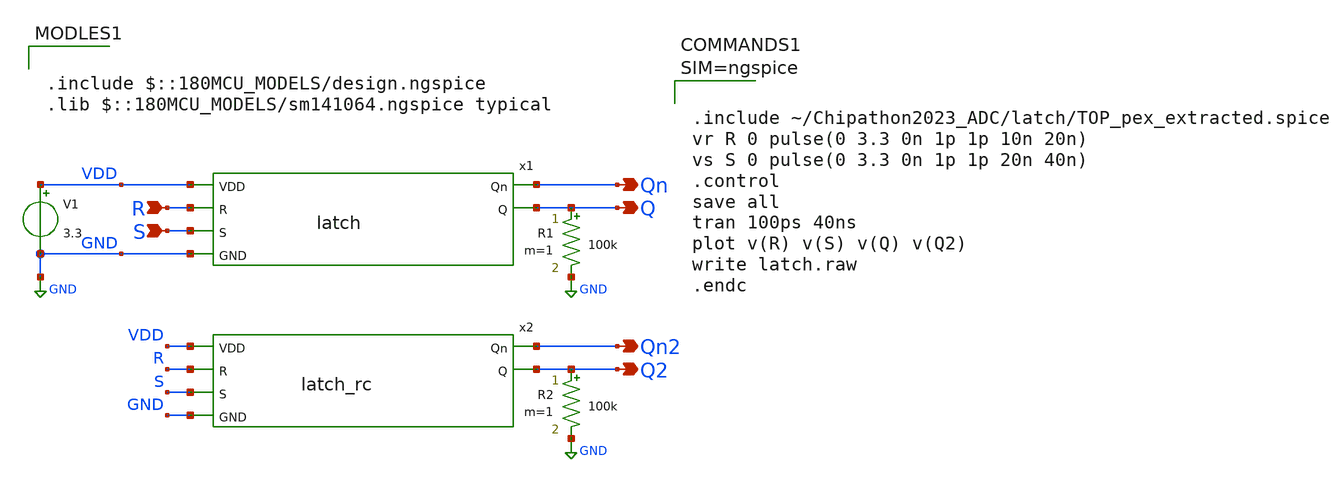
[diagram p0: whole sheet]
** sch_path: review/0407/latch/latch_rc_test.sch
**.subckt latch_rc_test Q R S Qn Q2 Qn2
*.opin Q
*.ipin R
*.ipin S
*.opin Qn
*.opin Q2
*.opin Qn2
x1 VDD Qn Q R S GND latch
V1 VDD GND 3.3
R1 Q GND 100k m=1
x2 S R VDD GND Qn2 Q2 TOP
R2 Q2 GND 100k m=1
**** begin user architecture code

.include $::180MCU_MODELS/design.ngspice
.lib $::180MCU_MODELS/sm141064.ngspice typical




.include ~/Chipathon2023_ADC/latch/TOP_pex_extracted.spice
vr R 0 pulse(0 3.3 0n 1p 1p 10n 20n)
vs S 0 pulse(0 3.3 0n 1p 1p 20n 40n)
.control
save all
tran 100ps 40ns
plot v(R) v(S) v(Q) v(Q2)
write latch.raw
.endc



**** end user architecture code
**.ends
.GLOBAL GND
.end
